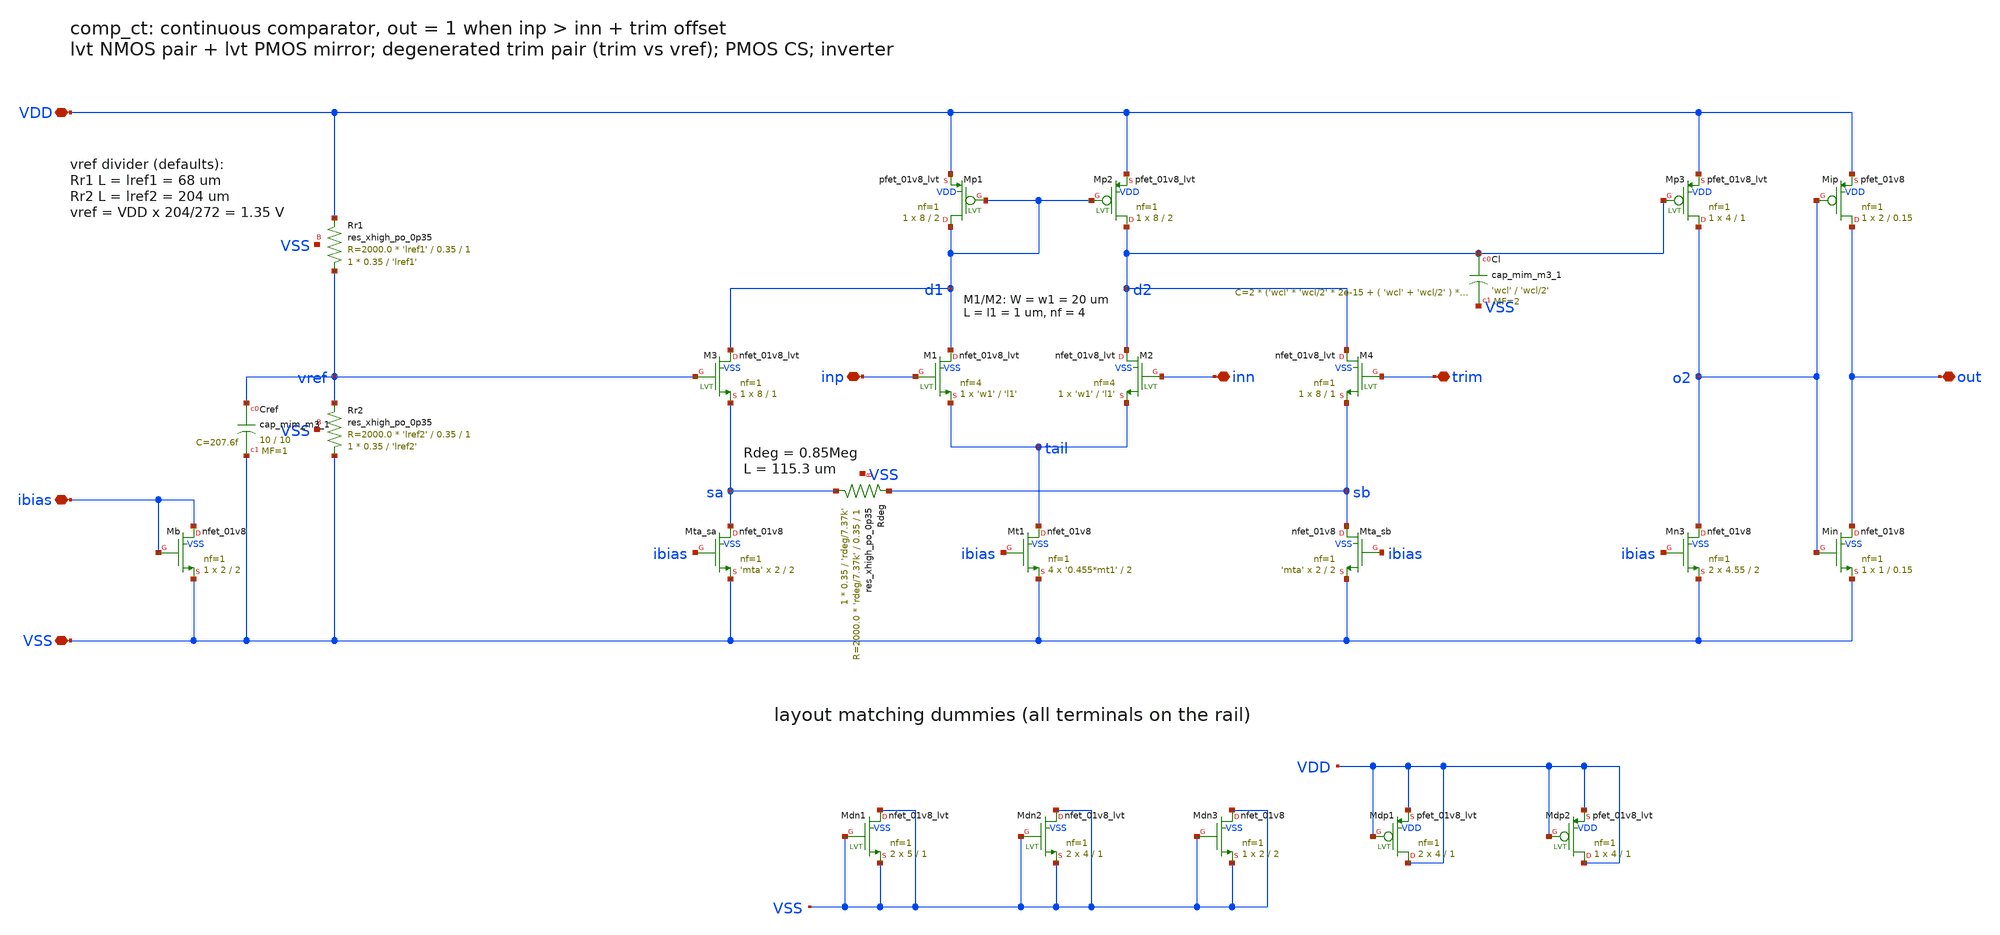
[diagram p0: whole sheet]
** sch_path: xschem/comp_ct.sch
**.subckt comp_ct VDD VSS ibias inp inn trim out
*.iopin VDD
*.iopin VSS
*.iopin ibias
*.iopin inp
*.iopin inn
*.iopin trim
*.iopin out
XMb ibias ibias VSS VSS sky130_fd_pr__nfet_01v8 L=2 W=2 nf=1 ad='int((nf+1)/2) * W/nf * 0.29' as='int((nf+2)/2) * W/nf * 0.29'
+ pd='2*int((nf+1)/2) * (W/nf + 0.29)' ps='2*int((nf+2)/2) * (W/nf + 0.29)' nrd='0.29 / W' nrs='0.29 / W'
+ sa=0 sb=0 sd=0 mult=1 m=1
XMt1 tail ibias VSS VSS sky130_fd_pr__nfet_01v8 L=2 W='0.455*mt1' nf=1 ad='int((nf+1)/2) * W/nf * 0.29'
+ as='int((nf+2)/2) * W/nf * 0.29' pd='2*int((nf+1)/2) * (W/nf + 0.29)' ps='2*int((nf+2)/2) * (W/nf + 0.29)'
+ nrd='0.29 / W' nrs='0.29 / W' sa=0 sb=0 sd=0 mult=4 m=4
XM1 d1 inp tail VSS sky130_fd_pr__nfet_01v8_lvt L='l1' W='w1' nf=4 ad='int((nf+1)/2) * W/nf * 0.29' as='int((nf+2)/2) * W/nf * 0.29'
+ pd='2*int((nf+1)/2) * (W/nf + 0.29)' ps='2*int((nf+2)/2) * (W/nf + 0.29)' nrd='0.29 / W' nrs='0.29 / W'
+ sa=0 sb=0 sd=0 mult=1 m=1
XM2 d2 inn tail VSS sky130_fd_pr__nfet_01v8_lvt L='l1' W='w1' nf=4 ad='int((nf+1)/2) * W/nf * 0.29' as='int((nf+2)/2) * W/nf * 0.29'
+ pd='2*int((nf+1)/2) * (W/nf + 0.29)' ps='2*int((nf+2)/2) * (W/nf + 0.29)' nrd='0.29 / W' nrs='0.29 / W'
+ sa=0 sb=0 sd=0 mult=1 m=1
XMp1 d1 d1 VDD VDD sky130_fd_pr__pfet_01v8_lvt L=2 W=8 nf=1 ad='int((nf+1)/2) * W/nf * 0.29' as='int((nf+2)/2) * W/nf * 0.29'
+ pd='2*int((nf+1)/2) * (W/nf + 0.29)' ps='2*int((nf+2)/2) * (W/nf + 0.29)' nrd='0.29 / W' nrs='0.29 / W'
+ sa=0 sb=0 sd=0 mult=1 m=1
XMp2 d2 d1 VDD VDD sky130_fd_pr__pfet_01v8_lvt L=2 W=8 nf=1 ad='int((nf+1)/2) * W/nf * 0.29' as='int((nf+2)/2) * W/nf * 0.29'
+ pd='2*int((nf+1)/2) * (W/nf + 0.29)' ps='2*int((nf+2)/2) * (W/nf + 0.29)' nrd='0.29 / W' nrs='0.29 / W'
+ sa=0 sb=0 sd=0 mult=1 m=1
XM3 d1 vref sa VSS sky130_fd_pr__nfet_01v8_lvt L=1 W=8 nf=1 ad='int((nf+1)/2) * W/nf * 0.29' as='int((nf+2)/2) * W/nf * 0.29'
+ pd='2*int((nf+1)/2) * (W/nf + 0.29)' ps='2*int((nf+2)/2) * (W/nf + 0.29)' nrd='0.29 / W' nrs='0.29 / W'
+ sa=0 sb=0 sd=0 mult=1 m=1
XMta_sa sa ibias VSS VSS sky130_fd_pr__nfet_01v8 L=2 W=2 nf=1 ad='int((nf+1)/2) * W/nf * 0.29' as='int((nf+2)/2) * W/nf * 0.29'
+ pd='2*int((nf+1)/2) * (W/nf + 0.29)' ps='2*int((nf+2)/2) * (W/nf + 0.29)' nrd='0.29 / W' nrs='0.29 / W'
+ sa=0 sb=0 sd=0 mult='mta' m='mta'
XM4 d2 trim sb VSS sky130_fd_pr__nfet_01v8_lvt L=1 W=8 nf=1 ad='int((nf+1)/2) * W/nf * 0.29' as='int((nf+2)/2) * W/nf * 0.29'
+ pd='2*int((nf+1)/2) * (W/nf + 0.29)' ps='2*int((nf+2)/2) * (W/nf + 0.29)' nrd='0.29 / W' nrs='0.29 / W'
+ sa=0 sb=0 sd=0 mult=1 m=1
XMta_sb sb ibias VSS VSS sky130_fd_pr__nfet_01v8 L=2 W=2 nf=1 ad='int((nf+1)/2) * W/nf * 0.29' as='int((nf+2)/2) * W/nf * 0.29'
+ pd='2*int((nf+1)/2) * (W/nf + 0.29)' ps='2*int((nf+2)/2) * (W/nf + 0.29)' nrd='0.29 / W' nrs='0.29 / W'
+ sa=0 sb=0 sd=0 mult='mta' m='mta'
XRdeg sa sb VSS sky130_fd_pr__res_xhigh_po_0p35 L='rdeg/7.37k' mult=1 m=1
XRr1 vref VDD VSS sky130_fd_pr__res_xhigh_po_0p35 L='lref1' mult=1 m=1
XRr2 VSS vref VSS sky130_fd_pr__res_xhigh_po_0p35 L='lref2' mult=1 m=1
XCref vref VSS sky130_fd_pr__cap_mim_m3_1 W=10 L=10 MF=1 m=1
XCl d2 VSS sky130_fd_pr__cap_mim_m3_1 W='wcl' L='wcl/2' MF=2 m=2
XMp3 o2 d2 VDD VDD sky130_fd_pr__pfet_01v8_lvt L=1 W=4 nf=1 ad='int((nf+1)/2) * W/nf * 0.29' as='int((nf+2)/2) * W/nf * 0.29'
+ pd='2*int((nf+1)/2) * (W/nf + 0.29)' ps='2*int((nf+2)/2) * (W/nf + 0.29)' nrd='0.29 / W' nrs='0.29 / W'
+ sa=0 sb=0 sd=0 mult=1 m=1
XMn3 o2 ibias VSS VSS sky130_fd_pr__nfet_01v8 L=2 W=4.55 nf=1 ad='int((nf+1)/2) * W/nf * 0.29' as='int((nf+2)/2) * W/nf * 0.29'
+ pd='2*int((nf+1)/2) * (W/nf + 0.29)' ps='2*int((nf+2)/2) * (W/nf + 0.29)' nrd='0.29 / W' nrs='0.29 / W'
+ sa=0 sb=0 sd=0 mult=2 m=2
XMip out o2 VDD VDD sky130_fd_pr__pfet_01v8 L=0.15 W=2 nf=1 ad='int((nf+1)/2) * W/nf * 0.29' as='int((nf+2)/2) * W/nf * 0.29'
+ pd='2*int((nf+1)/2) * (W/nf + 0.29)' ps='2*int((nf+2)/2) * (W/nf + 0.29)' nrd='0.29 / W' nrs='0.29 / W'
+ sa=0 sb=0 sd=0 mult=1 m=1
XMin out o2 VSS VSS sky130_fd_pr__nfet_01v8 L=0.15 W=1 nf=1 ad='int((nf+1)/2) * W/nf * 0.29' as='int((nf+2)/2) * W/nf * 0.29'
+ pd='2*int((nf+1)/2) * (W/nf + 0.29)' ps='2*int((nf+2)/2) * (W/nf + 0.29)' nrd='0.29 / W' nrs='0.29 / W'
+ sa=0 sb=0 sd=0 mult=1 m=1
XMdn1 VSS VSS VSS VSS sky130_fd_pr__nfet_01v8_lvt L=1 W=5 nf=1 ad='int((nf+1)/2) * W/nf * 0.29' as='int((nf+2)/2) * W/nf * 0.29'
+ pd='2*int((nf+1)/2) * (W/nf + 0.29)' ps='2*int((nf+2)/2) * (W/nf + 0.29)' nrd='0.29 / W' nrs='0.29 / W'
+ sa=0 sb=0 sd=0 mult=2 m=2
XMdn2 VSS VSS VSS VSS sky130_fd_pr__nfet_01v8_lvt L=1 W=4 nf=1 ad='int((nf+1)/2) * W/nf * 0.29' as='int((nf+2)/2) * W/nf * 0.29'
+ pd='2*int((nf+1)/2) * (W/nf + 0.29)' ps='2*int((nf+2)/2) * (W/nf + 0.29)' nrd='0.29 / W' nrs='0.29 / W'
+ sa=0 sb=0 sd=0 mult=2 m=2
XMdn3 VSS VSS VSS VSS sky130_fd_pr__nfet_01v8 L=2 W=2 nf=1 ad='int((nf+1)/2) * W/nf * 0.29' as='int((nf+2)/2) * W/nf * 0.29'
+ pd='2*int((nf+1)/2) * (W/nf + 0.29)' ps='2*int((nf+2)/2) * (W/nf + 0.29)' nrd='0.29 / W' nrs='0.29 / W'
+ sa=0 sb=0 sd=0 mult=1 m=1
XMdp1 VDD VDD VDD VDD sky130_fd_pr__pfet_01v8_lvt L=1 W=4 nf=1 ad='int((nf+1)/2) * W/nf * 0.29' as='int((nf+2)/2) * W/nf * 0.29'
+ pd='2*int((nf+1)/2) * (W/nf + 0.29)' ps='2*int((nf+2)/2) * (W/nf + 0.29)' nrd='0.29 / W' nrs='0.29 / W'
+ sa=0 sb=0 sd=0 mult=2 m=2
XMdp2 VDD VDD VDD VDD sky130_fd_pr__pfet_01v8_lvt L=1 W=4 nf=1 ad='int((nf+1)/2) * W/nf * 0.29' as='int((nf+2)/2) * W/nf * 0.29'
+ pd='2*int((nf+1)/2) * (W/nf + 0.29)' ps='2*int((nf+2)/2) * (W/nf + 0.29)' nrd='0.29 / W' nrs='0.29 / W'
+ sa=0 sb=0 sd=0 mult=1 m=1
**.ends
.end
